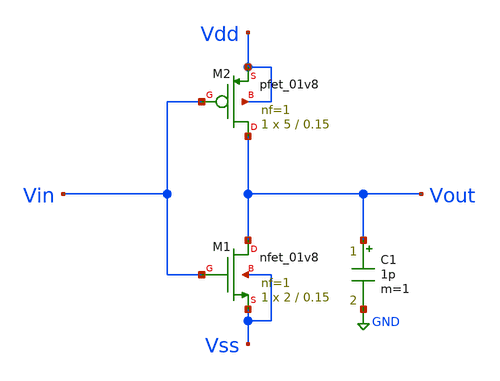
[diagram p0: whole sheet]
** sch_path: xschem/inverter_raw.sch
**.subckt inverter_raw
XM1 Vout Vin Vss Vss sky130_fd_pr__nfet_01v8 L=0.15 W=2 nf=1 ad='int((nf+1)/2) * W/nf * 0.29' as='int((nf+2)/2) * W/nf * 0.29'
+ pd='2*int((nf+1)/2) * (W/nf + 0.29)' ps='2*int((nf+2)/2) * (W/nf + 0.29)' nrd='0.29 / W' nrs='0.29 / W'
+ sa=0 sb=0 sd=0 mult=1 m=1
XM2 Vout Vin Vdd Vdd sky130_fd_pr__pfet_01v8 L=0.15 W=5 nf=1 ad='int((nf+1)/2) * W/nf * 0.29' as='int((nf+2)/2) * W/nf * 0.29'
+ pd='2*int((nf+1)/2) * (W/nf + 0.29)' ps='2*int((nf+2)/2) * (W/nf + 0.29)' nrd='0.29 / W' nrs='0.29 / W'
+ sa=0 sb=0 sd=0 mult=1 m=1
C1 Vout GND 1p m=1
**.ends
.GLOBAL GND
.end
